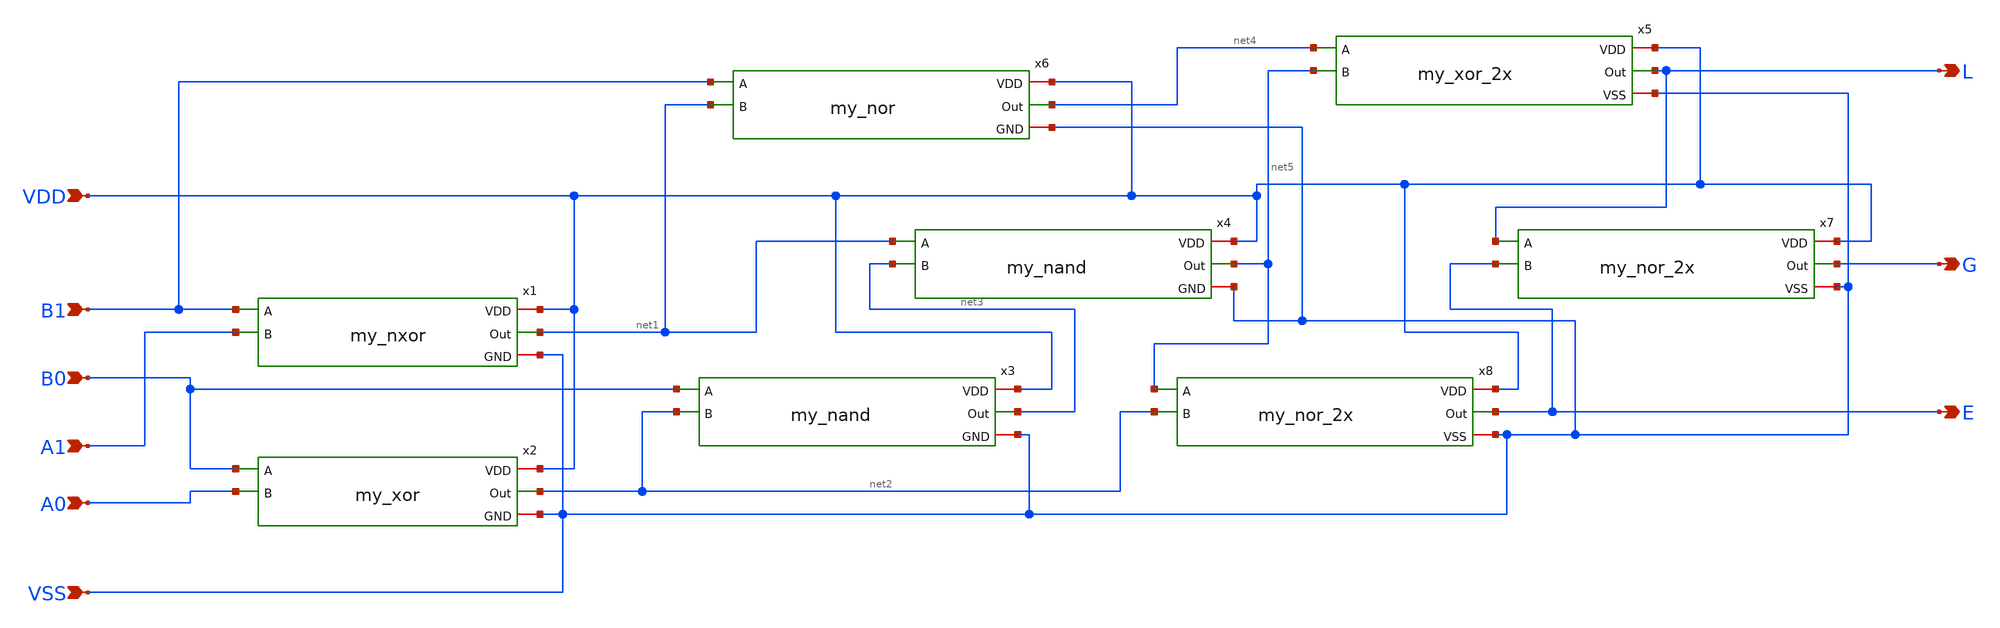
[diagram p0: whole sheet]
** sch_path: cells/comp4/2x_drive_v2/2bit_comp_2x.sch
**.subckt 2bit_comp_2x VDD B1 B0 A1 VSS A0 L G E
*.ipin VDD
*.ipin B1
*.ipin B0
*.ipin A1
*.ipin VSS
*.ipin A0
*.opin L
*.opin G
*.opin E
x1 VDD B1 net1 A1 VSS my_nxor
x2 VDD B0 net2 A0 VSS my_xor
x3 VDD B0 net2 net3 VSS my_nand
x4 VDD net1 net3 net5 VSS my_nand
x6 VDD B1 net1 net4 VSS my_nor
x5 VDD net4 L net5 VSS my_xor_2x
x7 VDD L E G VSS my_nor_2x
x8 VDD net5 net2 E VSS my_nor_2x
**.ends
.end
